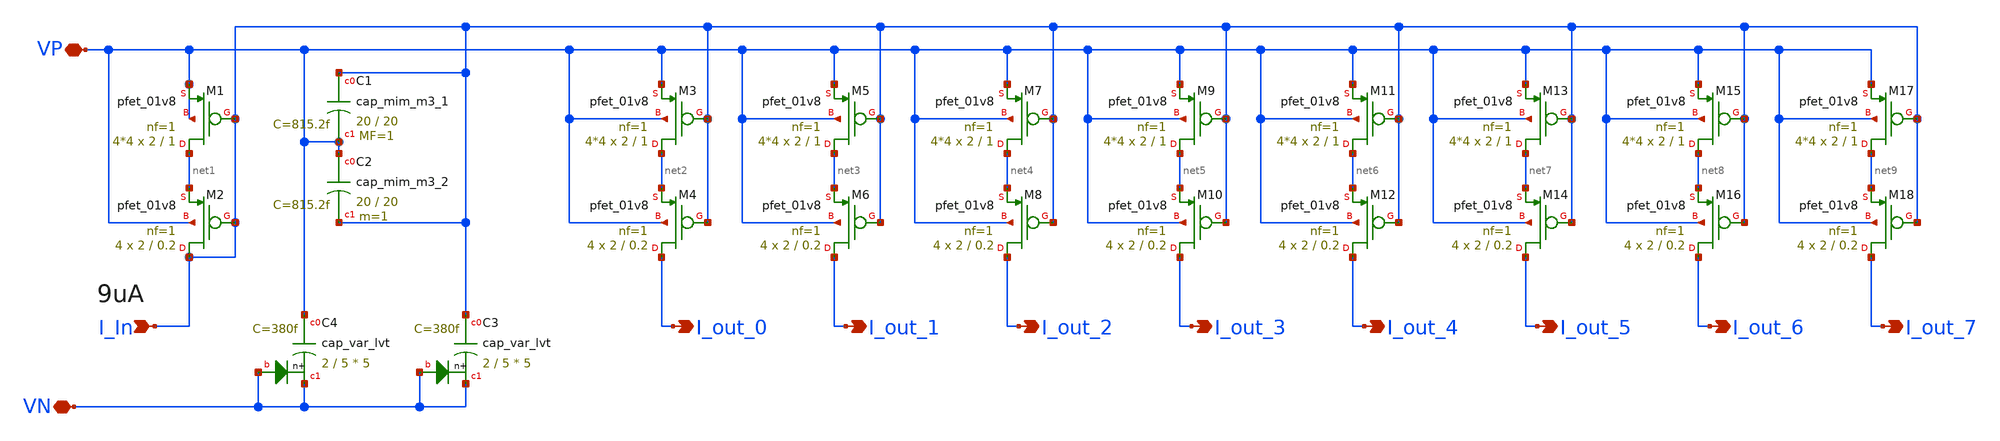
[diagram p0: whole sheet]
** sch_path: xschem/bias/current_mirrorx8.sch
**.subckt current_mirrorx8 I_out_0 I_In VP I_out_1 I_out_2 I_out_3 I_out_4 I_out_5 I_out_6 I_out_7
*+ VN
*.opin I_out_0
*.ipin I_In
*.iopin VP
*.opin I_out_1
*.opin I_out_2
*.opin I_out_3
*.opin I_out_4
*.opin I_out_5
*.opin I_out_6
*.opin I_out_7
*.iopin VN
XM1 net1 I_In VP VP sky130_fd_pr__pfet_01v8 L=1 W=2 nf=1 ad='int((nf+1)/2) * W/nf * 0.29' as='int((nf+2)/2) * W/nf * 0.29'
+ pd='2*int((nf+1)/2) * (W/nf + 0.29)' ps='2*int((nf+2)/2) * (W/nf + 0.29)' nrd='0.29 / W' nrs='0.29 / W'
+ sa=0 sb=0 sd=0 mult=4*4 m=4*4
XM2 I_In I_In net1 VP sky130_fd_pr__pfet_01v8 L=0.2 W=2 nf=1 ad='int((nf+1)/2) * W/nf * 0.29' as='int((nf+2)/2) * W/nf * 0.29'
+ pd='2*int((nf+1)/2) * (W/nf + 0.29)' ps='2*int((nf+2)/2) * (W/nf + 0.29)' nrd='0.29 / W' nrs='0.29 / W'
+ sa=0 sb=0 sd=0 mult=4 m=4
XC1 I_In VP sky130_fd_pr__cap_mim_m3_1 W=20 L=20 MF=1 m=1
XC2 VP I_In sky130_fd_pr__cap_mim_m3_2 W=20 L=20 MF=1 m=1
XC4 VP VN VN sky130_fd_pr__cap_var_lvt W=2 L=5 VM=5 m=5
XC3 I_In VN VN sky130_fd_pr__cap_var_lvt W=2 L=5 VM=5 m=5
XM3 net2 I_In VP VP sky130_fd_pr__pfet_01v8 L=1 W=2 nf=1 ad='int((nf+1)/2) * W/nf * 0.29' as='int((nf+2)/2) * W/nf * 0.29'
+ pd='2*int((nf+1)/2) * (W/nf + 0.29)' ps='2*int((nf+2)/2) * (W/nf + 0.29)' nrd='0.29 / W' nrs='0.29 / W'
+ sa=0 sb=0 sd=0 mult=4*4 m=4*4
XM4 I_out_0 I_In net2 VP sky130_fd_pr__pfet_01v8 L=0.2 W=2 nf=1 ad='int((nf+1)/2) * W/nf * 0.29' as='int((nf+2)/2) * W/nf * 0.29'
+ pd='2*int((nf+1)/2) * (W/nf + 0.29)' ps='2*int((nf+2)/2) * (W/nf + 0.29)' nrd='0.29 / W' nrs='0.29 / W'
+ sa=0 sb=0 sd=0 mult=4 m=4
XM5 net3 I_In VP VP sky130_fd_pr__pfet_01v8 L=1 W=2 nf=1 ad='int((nf+1)/2) * W/nf * 0.29' as='int((nf+2)/2) * W/nf * 0.29'
+ pd='2*int((nf+1)/2) * (W/nf + 0.29)' ps='2*int((nf+2)/2) * (W/nf + 0.29)' nrd='0.29 / W' nrs='0.29 / W'
+ sa=0 sb=0 sd=0 mult=4*4 m=4*4
XM6 I_out_1 I_In net3 VP sky130_fd_pr__pfet_01v8 L=0.2 W=2 nf=1 ad='int((nf+1)/2) * W/nf * 0.29' as='int((nf+2)/2) * W/nf * 0.29'
+ pd='2*int((nf+1)/2) * (W/nf + 0.29)' ps='2*int((nf+2)/2) * (W/nf + 0.29)' nrd='0.29 / W' nrs='0.29 / W'
+ sa=0 sb=0 sd=0 mult=4 m=4
XM7 net4 I_In VP VP sky130_fd_pr__pfet_01v8 L=1 W=2 nf=1 ad='int((nf+1)/2) * W/nf * 0.29' as='int((nf+2)/2) * W/nf * 0.29'
+ pd='2*int((nf+1)/2) * (W/nf + 0.29)' ps='2*int((nf+2)/2) * (W/nf + 0.29)' nrd='0.29 / W' nrs='0.29 / W'
+ sa=0 sb=0 sd=0 mult=4*4 m=4*4
XM8 I_out_2 I_In net4 VP sky130_fd_pr__pfet_01v8 L=0.2 W=2 nf=1 ad='int((nf+1)/2) * W/nf * 0.29' as='int((nf+2)/2) * W/nf * 0.29'
+ pd='2*int((nf+1)/2) * (W/nf + 0.29)' ps='2*int((nf+2)/2) * (W/nf + 0.29)' nrd='0.29 / W' nrs='0.29 / W'
+ sa=0 sb=0 sd=0 mult=4 m=4
XM9 net5 I_In VP VP sky130_fd_pr__pfet_01v8 L=1 W=2 nf=1 ad='int((nf+1)/2) * W/nf * 0.29' as='int((nf+2)/2) * W/nf * 0.29'
+ pd='2*int((nf+1)/2) * (W/nf + 0.29)' ps='2*int((nf+2)/2) * (W/nf + 0.29)' nrd='0.29 / W' nrs='0.29 / W'
+ sa=0 sb=0 sd=0 mult=4*4 m=4*4
XM10 I_out_3 I_In net5 VP sky130_fd_pr__pfet_01v8 L=0.2 W=2 nf=1 ad='int((nf+1)/2) * W/nf * 0.29' as='int((nf+2)/2) * W/nf * 0.29'
+ pd='2*int((nf+1)/2) * (W/nf + 0.29)' ps='2*int((nf+2)/2) * (W/nf + 0.29)' nrd='0.29 / W' nrs='0.29 / W'
+ sa=0 sb=0 sd=0 mult=4 m=4
XM11 net6 I_In VP VP sky130_fd_pr__pfet_01v8 L=1 W=2 nf=1 ad='int((nf+1)/2) * W/nf * 0.29' as='int((nf+2)/2) * W/nf * 0.29'
+ pd='2*int((nf+1)/2) * (W/nf + 0.29)' ps='2*int((nf+2)/2) * (W/nf + 0.29)' nrd='0.29 / W' nrs='0.29 / W'
+ sa=0 sb=0 sd=0 mult=4*4 m=4*4
XM12 I_out_4 I_In net6 VP sky130_fd_pr__pfet_01v8 L=0.2 W=2 nf=1 ad='int((nf+1)/2) * W/nf * 0.29' as='int((nf+2)/2) * W/nf * 0.29'
+ pd='2*int((nf+1)/2) * (W/nf + 0.29)' ps='2*int((nf+2)/2) * (W/nf + 0.29)' nrd='0.29 / W' nrs='0.29 / W'
+ sa=0 sb=0 sd=0 mult=4 m=4
XM13 net7 I_In VP VP sky130_fd_pr__pfet_01v8 L=1 W=2 nf=1 ad='int((nf+1)/2) * W/nf * 0.29' as='int((nf+2)/2) * W/nf * 0.29'
+ pd='2*int((nf+1)/2) * (W/nf + 0.29)' ps='2*int((nf+2)/2) * (W/nf + 0.29)' nrd='0.29 / W' nrs='0.29 / W'
+ sa=0 sb=0 sd=0 mult=4*4 m=4*4
XM14 I_out_5 I_In net7 VP sky130_fd_pr__pfet_01v8 L=0.2 W=2 nf=1 ad='int((nf+1)/2) * W/nf * 0.29' as='int((nf+2)/2) * W/nf * 0.29'
+ pd='2*int((nf+1)/2) * (W/nf + 0.29)' ps='2*int((nf+2)/2) * (W/nf + 0.29)' nrd='0.29 / W' nrs='0.29 / W'
+ sa=0 sb=0 sd=0 mult=4 m=4
XM15 net8 I_In VP VP sky130_fd_pr__pfet_01v8 L=1 W=2 nf=1 ad='int((nf+1)/2) * W/nf * 0.29' as='int((nf+2)/2) * W/nf * 0.29'
+ pd='2*int((nf+1)/2) * (W/nf + 0.29)' ps='2*int((nf+2)/2) * (W/nf + 0.29)' nrd='0.29 / W' nrs='0.29 / W'
+ sa=0 sb=0 sd=0 mult=4*4 m=4*4
XM16 I_out_6 I_In net8 VP sky130_fd_pr__pfet_01v8 L=0.2 W=2 nf=1 ad='int((nf+1)/2) * W/nf * 0.29' as='int((nf+2)/2) * W/nf * 0.29'
+ pd='2*int((nf+1)/2) * (W/nf + 0.29)' ps='2*int((nf+2)/2) * (W/nf + 0.29)' nrd='0.29 / W' nrs='0.29 / W'
+ sa=0 sb=0 sd=0 mult=4 m=4
XM17 net9 I_In VP VP sky130_fd_pr__pfet_01v8 L=1 W=2 nf=1 ad='int((nf+1)/2) * W/nf * 0.29' as='int((nf+2)/2) * W/nf * 0.29'
+ pd='2*int((nf+1)/2) * (W/nf + 0.29)' ps='2*int((nf+2)/2) * (W/nf + 0.29)' nrd='0.29 / W' nrs='0.29 / W'
+ sa=0 sb=0 sd=0 mult=4*4 m=4*4
XM18 I_out_7 I_In net9 VP sky130_fd_pr__pfet_01v8 L=0.2 W=2 nf=1 ad='int((nf+1)/2) * W/nf * 0.29' as='int((nf+2)/2) * W/nf * 0.29'
+ pd='2*int((nf+1)/2) * (W/nf + 0.29)' ps='2*int((nf+2)/2) * (W/nf + 0.29)' nrd='0.29 / W' nrs='0.29 / W'
+ sa=0 sb=0 sd=0 mult=4 m=4
**.ends
.end
